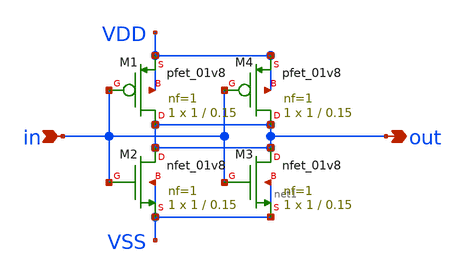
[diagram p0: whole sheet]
** sch_path: archive/tt_um_wulf_8bit_vco/xschem/lib/buf_sm.sch
**.subckt buf_sm out in
*.opin out
*.ipin in
XM2 out in VSS VSS sky130_fd_pr__nfet_01v8 L=0.15 W=1 nf=1 ad='int((1 + 1)/2) * 1 / 1 * 0.29' as='int((1 + 2)/2) * 1 / 1 * 0.29'
+ pd='2*int((1 + 1)/2) * (1 / 1 + 0.29)' ps='2*int((1 + 2)/2) * (1 / 1 + 0.29)' nrd='0.29 / 1 ' nrs='0.29 / 1 '
+ sa=0 sb=0 sd=0 mult=1 m=1
XM1 out in VDD VDD sky130_fd_pr__pfet_01v8 L=0.15 W=1 nf=1 ad='int((nf+1)/2) * W/nf * 0.29' as='int((nf+2)/2) * W/nf * 0.29'
+ pd='2*int((nf+1)/2) * (W/nf + 0.29)' ps='2*int((nf+2)/2) * (W/nf + 0.29)' nrd='0.29 / W' nrs='0.29 / W'
+ sa=0 sb=0 sd=0 mult=1 m=1
XM3 out in VSS net1 sky130_fd_pr__nfet_01v8 L=0.15 W=1 nf=1 ad='int((1 + 1)/2) * 1 / 1 * 0.29' as='int((1 + 2)/2) * 1 / 1 * 0.29'
+ pd='2*int((1 + 1)/2) * (1 / 1 + 0.29)' ps='2*int((1 + 2)/2) * (1 / 1 + 0.29)' nrd='0.29 / 1 ' nrs='0.29 / 1 '
+ sa=0 sb=0 sd=0 mult=1 m=1
XM4 out in VDD VDD sky130_fd_pr__pfet_01v8 L=0.15 W=1 nf=1 ad='int((nf+1)/2) * W/nf * 0.29' as='int((nf+2)/2) * W/nf * 0.29'
+ pd='2*int((nf+1)/2) * (W/nf + 0.29)' ps='2*int((nf+2)/2) * (W/nf + 0.29)' nrd='0.29 / W' nrs='0.29 / W'
+ sa=0 sb=0 sd=0 mult=1 m=1
**.ends
.end
